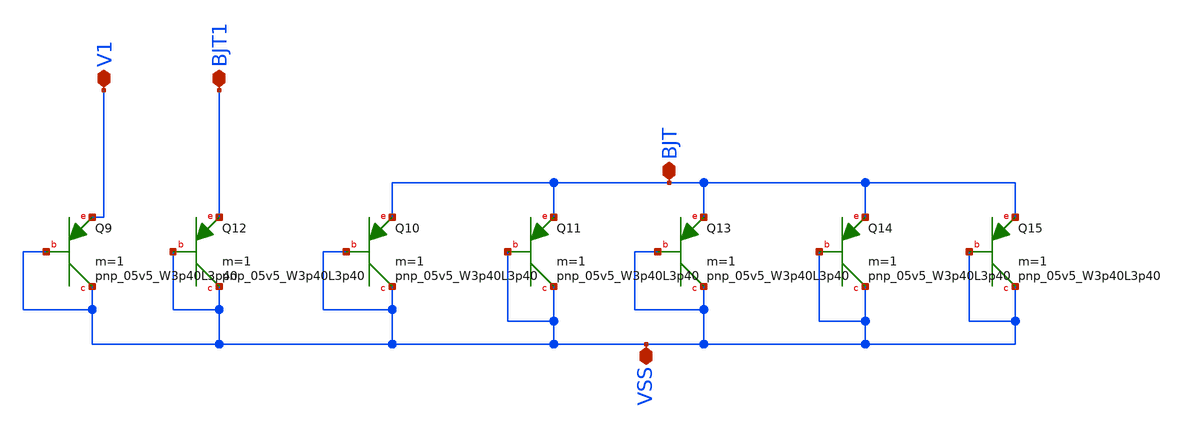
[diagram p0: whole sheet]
** sch_path: xschem/xschem_BGR_Top/BJTs.sch
**.subckt BJTs VSS BJT BJT1 V1
*.iopin VSS
*.iopin BJT
*.iopin BJT1
*.iopin V1
XQ10 VSS VSS BJT sky130_fd_pr__pnp_05v5_W3p40L3p40 m=1
XQ11 VSS VSS BJT sky130_fd_pr__pnp_05v5_W3p40L3p40 m=1
XQ13 VSS VSS BJT sky130_fd_pr__pnp_05v5_W3p40L3p40 m=1
XQ14 VSS VSS BJT sky130_fd_pr__pnp_05v5_W3p40L3p40 m=1
XQ15 VSS VSS BJT sky130_fd_pr__pnp_05v5_W3p40L3p40 m=1
XQ12 VSS VSS BJT1 sky130_fd_pr__pnp_05v5_W3p40L3p40 m=1
XQ9 VSS VSS V1 sky130_fd_pr__pnp_05v5_W3p40L3p40 m=1
**.ends
.end
